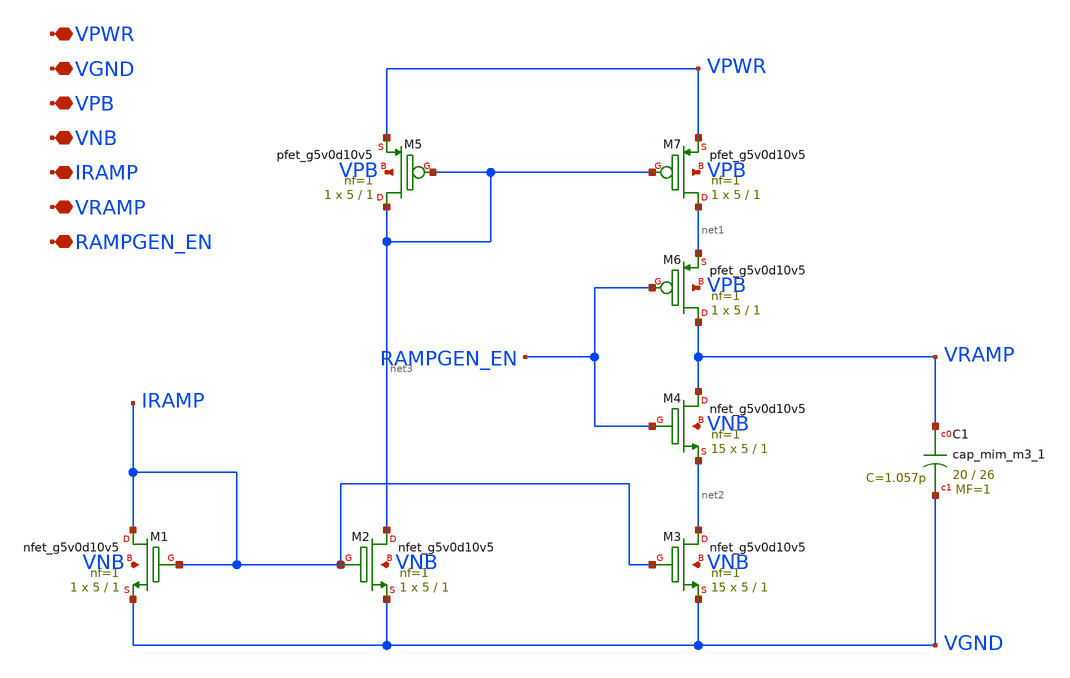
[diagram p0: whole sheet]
** sch_path: design/oscillator/rampgen.sch
**.subckt rampgen VPWR VGND VPB VNB IRAMP VRAMP RAMPGEN_EN
*.iopin VPWR
*.iopin VGND
*.iopin VPB
*.iopin VNB
*.iopin IRAMP
*.iopin VRAMP
*.iopin RAMPGEN_EN
XM1 IRAMP IRAMP VGND VNB sky130_fd_pr__nfet_g5v0d10v5 L=1 W=5 nf=1 ad='int((nf+1)/2) * W/nf * 0.29' as='int((nf+2)/2) * W/nf * 0.29'
+ pd='2*int((nf+1)/2) * (W/nf + 0.29)' ps='2*int((nf+2)/2) * (W/nf + 0.29)' nrd='0.29 / W' nrs='0.29 / W'
+ sa=0 sb=0 sd=0 mult=1 m=1
XM2 net3 IRAMP VGND VNB sky130_fd_pr__nfet_g5v0d10v5 L=1 W=5 nf=1 ad='int((nf+1)/2) * W/nf * 0.29' as='int((nf+2)/2) * W/nf * 0.29'
+ pd='2*int((nf+1)/2) * (W/nf + 0.29)' ps='2*int((nf+2)/2) * (W/nf + 0.29)' nrd='0.29 / W' nrs='0.29 / W'
+ sa=0 sb=0 sd=0 mult=1 m=1
XM3 net2 IRAMP VGND VNB sky130_fd_pr__nfet_g5v0d10v5 L=1 W=5 nf=1 ad='int((nf+1)/2) * W/nf * 0.29' as='int((nf+2)/2) * W/nf * 0.29'
+ pd='2*int((nf+1)/2) * (W/nf + 0.29)' ps='2*int((nf+2)/2) * (W/nf + 0.29)' nrd='0.29 / W' nrs='0.29 / W'
+ sa=0 sb=0 sd=0 mult=15 m=15
XM4 VRAMP RAMPGEN_EN net2 VNB sky130_fd_pr__nfet_g5v0d10v5 L=1 W=5 nf=1 ad='int((nf+1)/2) * W/nf * 0.29'
+ as='int((nf+2)/2) * W/nf * 0.29' pd='2*int((nf+1)/2) * (W/nf + 0.29)' ps='2*int((nf+2)/2) * (W/nf + 0.29)'
+ nrd='0.29 / W' nrs='0.29 / W' sa=0 sb=0 sd=0 mult=15 m=15
XM5 net3 net3 VPWR VPB sky130_fd_pr__pfet_g5v0d10v5 L=1 W=5 nf=1 ad='int((nf+1)/2) * W/nf * 0.29' as='int((nf+2)/2) * W/nf * 0.29'
+ pd='2*int((nf+1)/2) * (W/nf + 0.29)' ps='2*int((nf+2)/2) * (W/nf + 0.29)' nrd='0.29 / W' nrs='0.29 / W'
+ sa=0 sb=0 sd=0 mult=1 m=1
XM6 VRAMP RAMPGEN_EN net1 VPB sky130_fd_pr__pfet_g5v0d10v5 L=1 W=5 nf=1 ad='int((nf+1)/2) * W/nf * 0.29'
+ as='int((nf+2)/2) * W/nf * 0.29' pd='2*int((nf+1)/2) * (W/nf + 0.29)' ps='2*int((nf+2)/2) * (W/nf + 0.29)'
+ nrd='0.29 / W' nrs='0.29 / W' sa=0 sb=0 sd=0 mult=1 m=1
XM7 net1 net3 VPWR VPB sky130_fd_pr__pfet_g5v0d10v5 L=1 W=5 nf=1 ad='int((nf+1)/2) * W/nf * 0.29' as='int((nf+2)/2) * W/nf * 0.29'
+ pd='2*int((nf+1)/2) * (W/nf + 0.29)' ps='2*int((nf+2)/2) * (W/nf + 0.29)' nrd='0.29 / W' nrs='0.29 / W'
+ sa=0 sb=0 sd=0 mult=1 m=1
XC1 VRAMP VGND sky130_fd_pr__cap_mim_m3_1 W=20 L=26 MF=1 m=1
**.ends
.end
